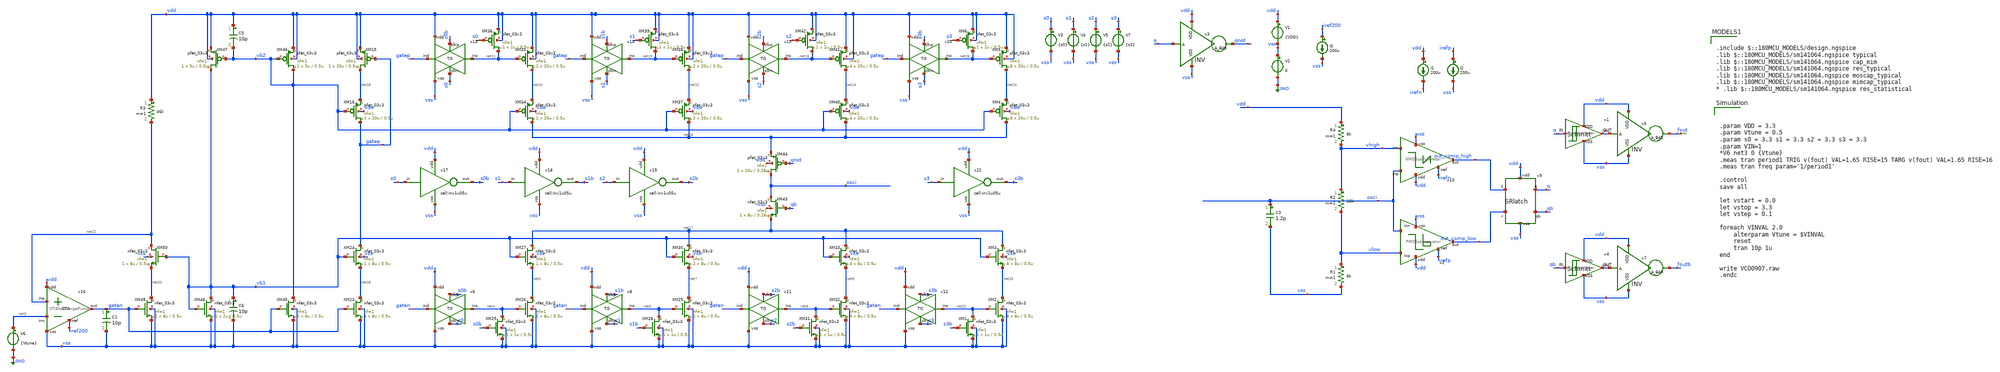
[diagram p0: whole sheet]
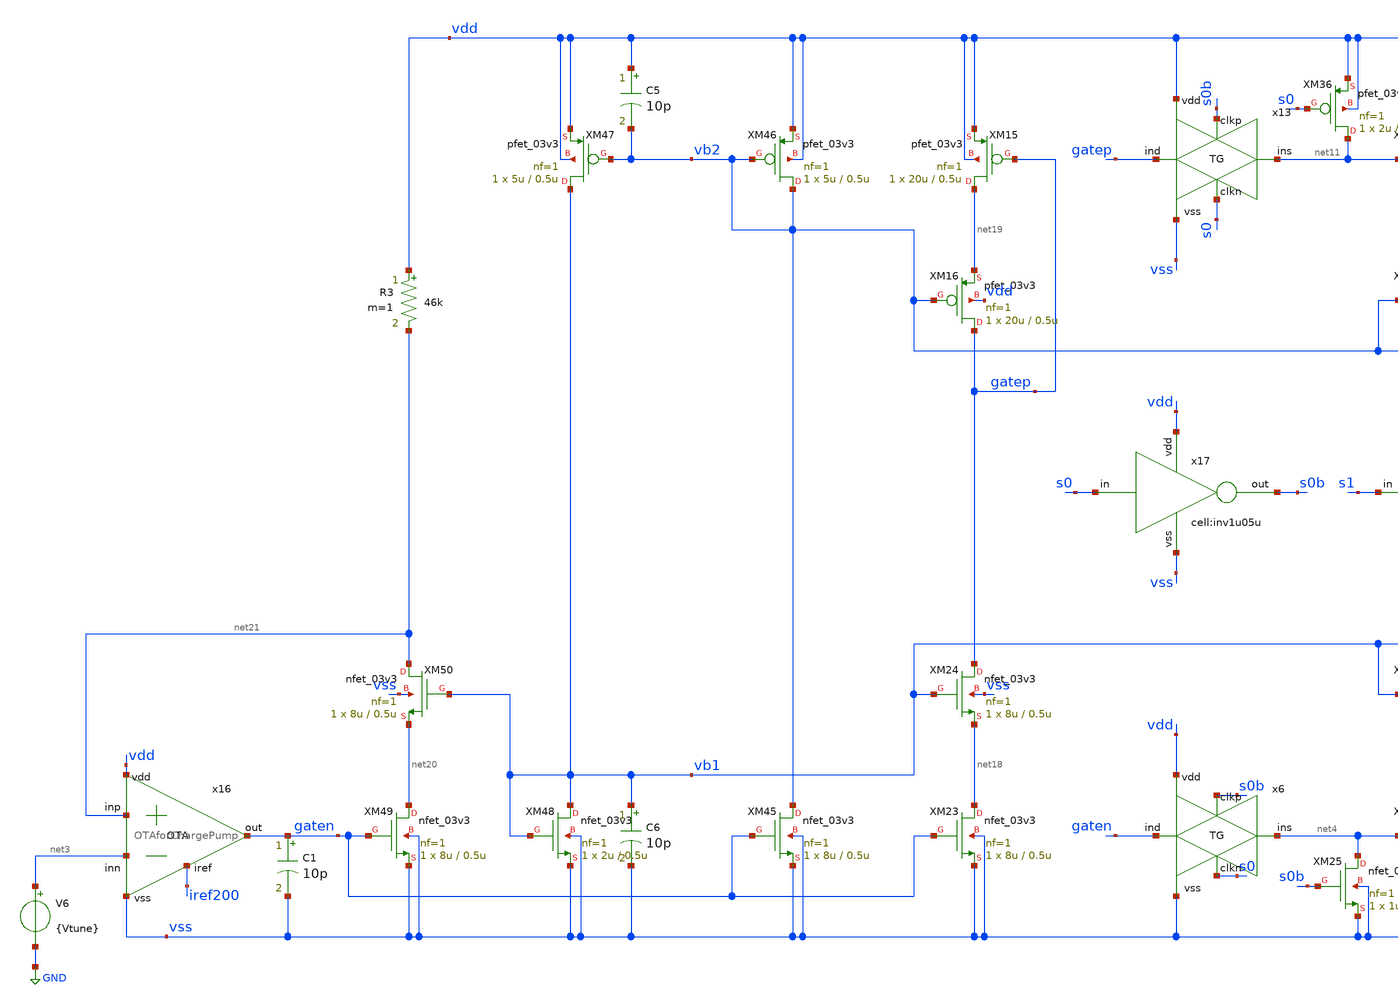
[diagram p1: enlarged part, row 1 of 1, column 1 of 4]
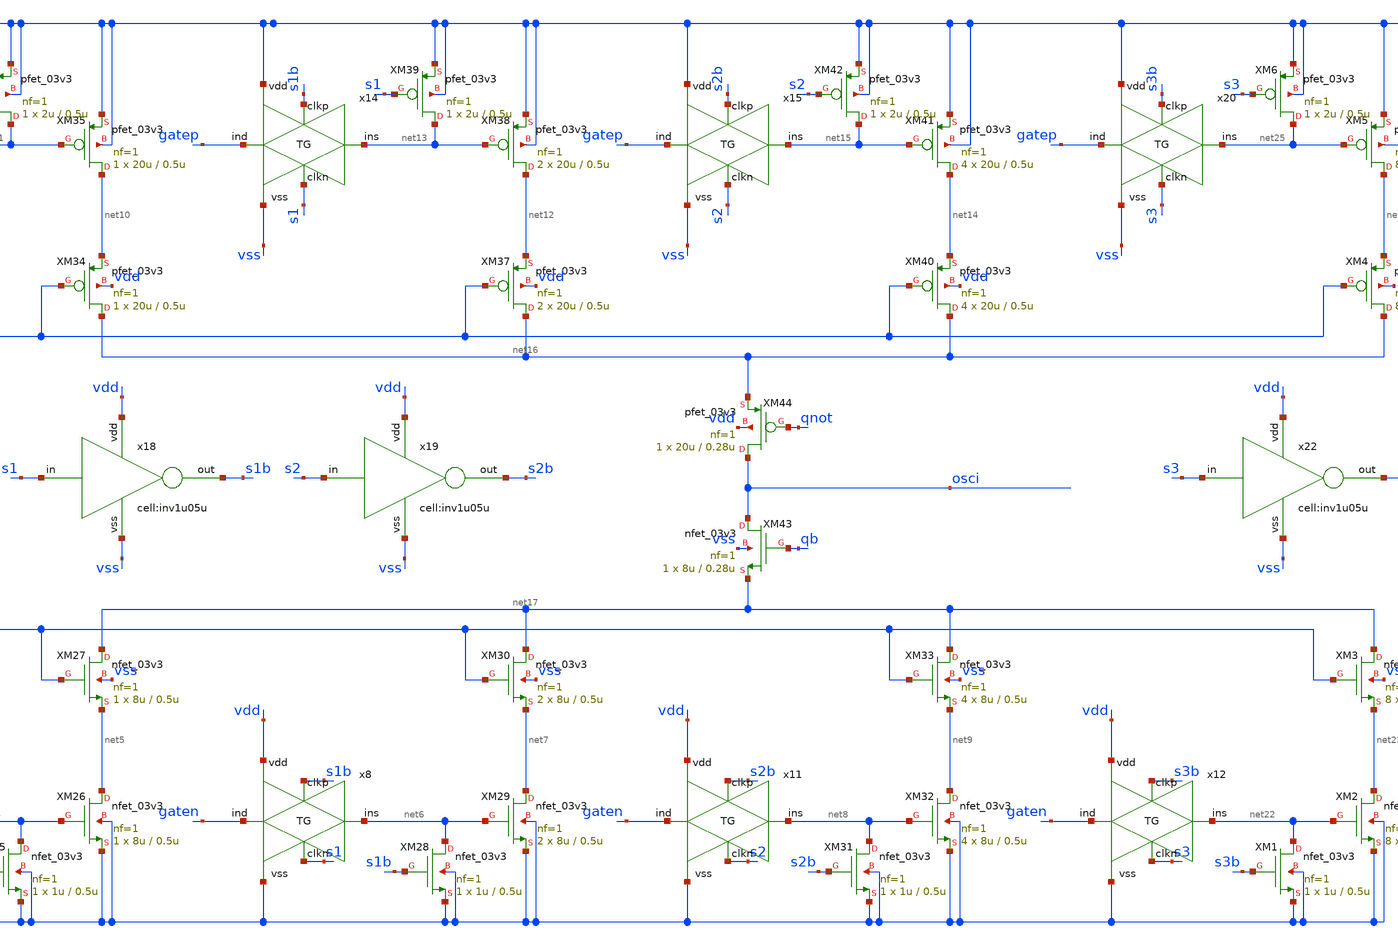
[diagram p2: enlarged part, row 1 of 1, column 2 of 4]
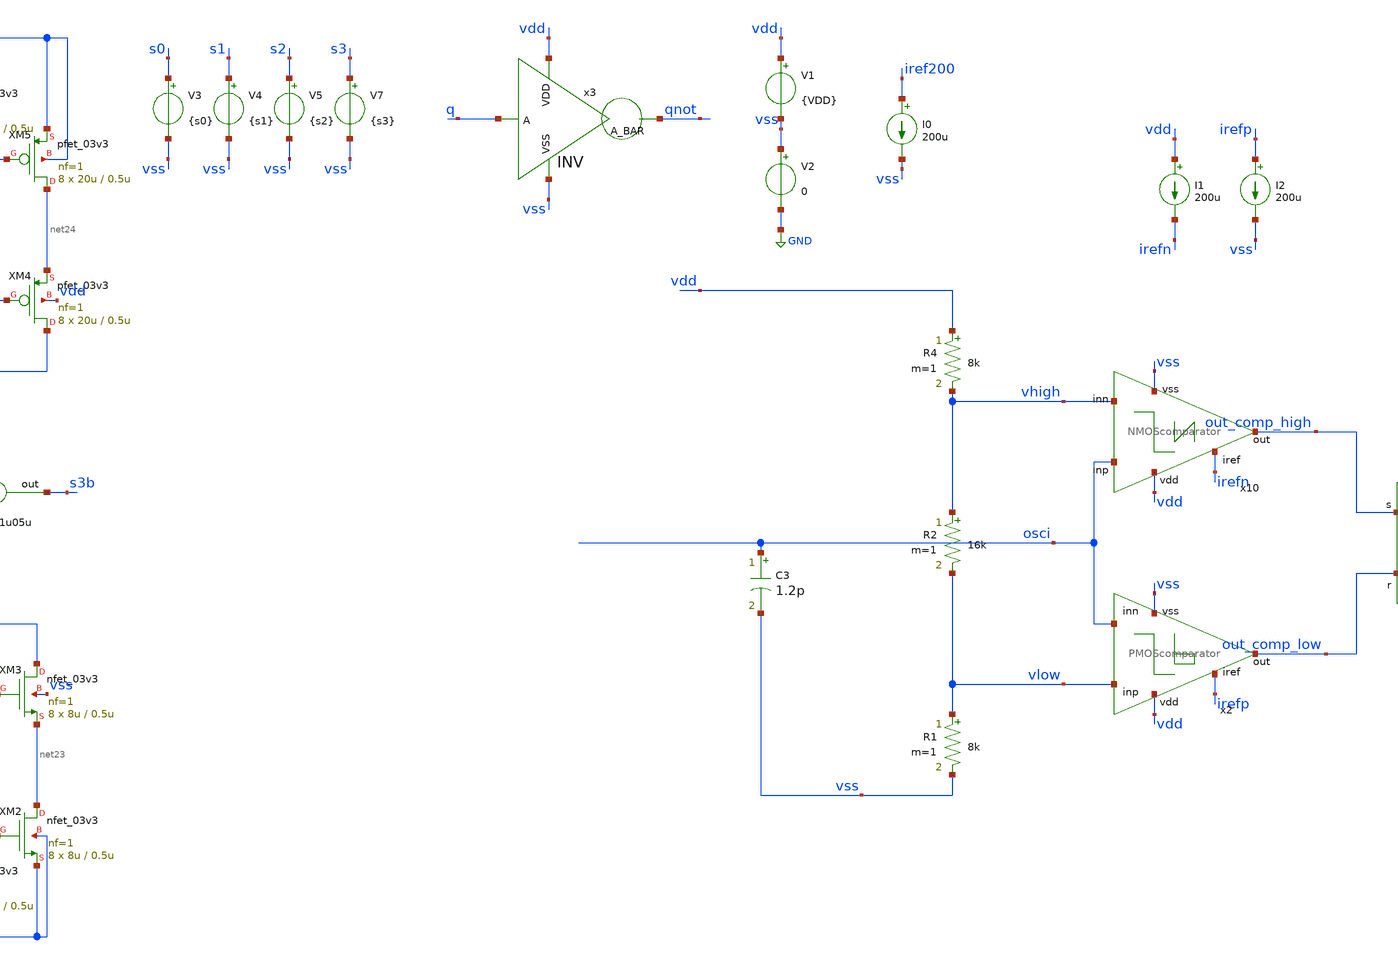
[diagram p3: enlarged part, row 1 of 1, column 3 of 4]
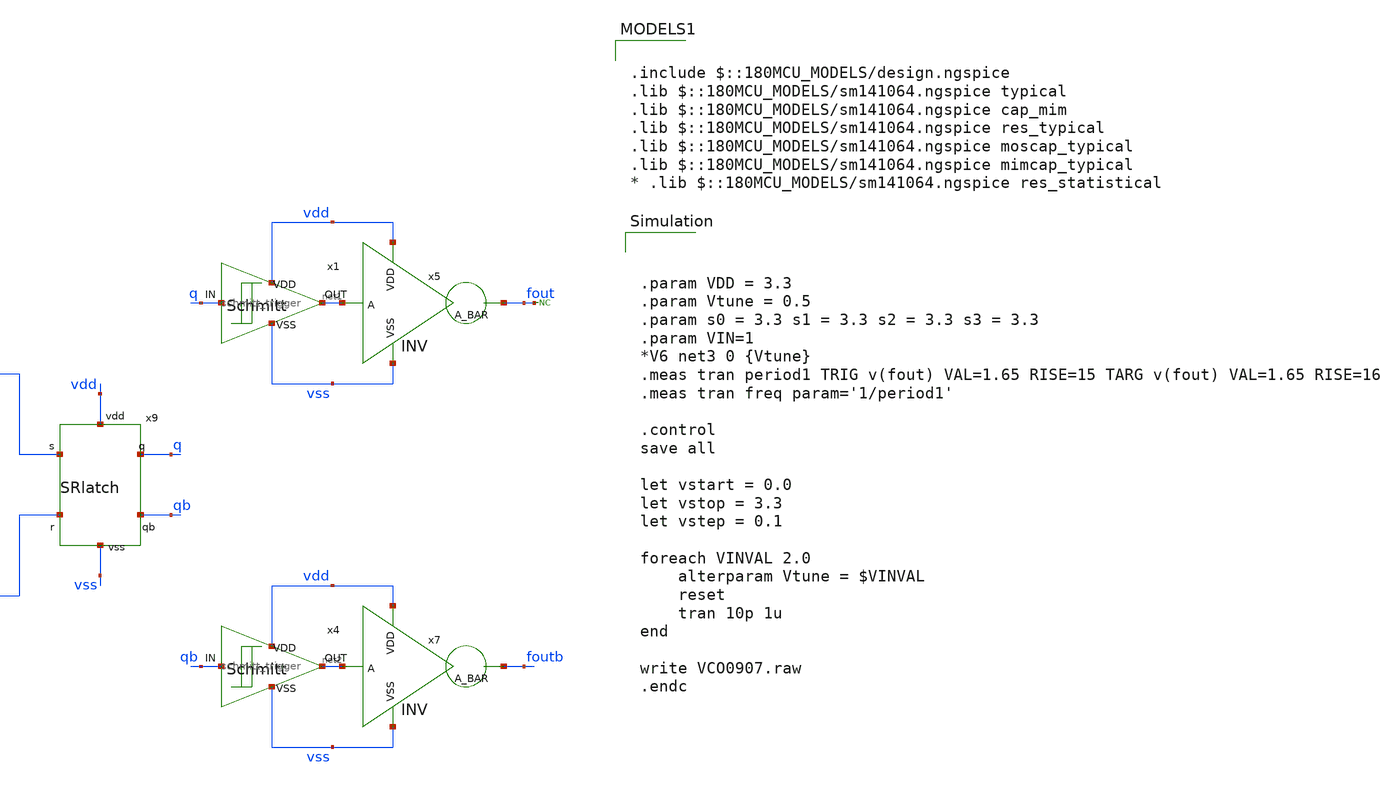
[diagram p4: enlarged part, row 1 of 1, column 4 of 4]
** sch_path: designs/libs/qw_tb_analog/VCOfinal_tb/VCOfinal_tb.sch
**.subckt VCOfinal_tb
V1 vdd vss {VDD}
V2 vss GND 0
I1 vdd irefn 200u
I2 irefp vss 200u
R1 vlow vss 8k m=1
R2 vhigh vlow 16k m=1
R4 vdd vhigh 8k m=1
x9 vdd out_comp_high q qb out_comp_low vss SRlatch
x2 vdd irefp vlow out_comp_low osci vss PMOScomparator
x10 vdd osci out_comp_high vhigh irefn vss NMOScomparator
x3 vdd q qnot vss INV
x1 q net1 vdd vss schmitt_trigger
x4 qb net2 vdd vss schmitt_trigger
x5 vdd net1 fout vss INV
x7 vdd net2 foutb vss INV
V6 net3 GND {Vtune}
I0 iref200 vss 200u
* noconn fout
V3 s0 vss {s0}
V4 s1 vss {s1}
V5 s2 vss {s2}
C3 osci vss 1.2p m=1
V7 s3 vss {s3}
XM25 net4 s0b vss vss nfet_03v3 L=0.5u W=1u nf=1 ad='int((nf+1)/2) * W/nf * 0.18u' as='int((nf+2)/2) * W/nf * 0.18u'
+ pd='2*int((nf+1)/2) * (W/nf + 0.18u)' ps='2*int((nf+2)/2) * (W/nf + 0.18u)' nrd='0.18u / W' nrs='0.18u / W'
+ sa=0 sb=0 sd=0 m=1
XM26 net5 net4 vss vss nfet_03v3 L=0.5u W=8u nf=1 ad='int((nf+1)/2) * W/nf * 0.18u' as='int((nf+2)/2) * W/nf * 0.18u'
+ pd='2*int((nf+1)/2) * (W/nf + 0.18u)' ps='2*int((nf+2)/2) * (W/nf + 0.18u)' nrd='0.18u / W' nrs='0.18u / W'
+ sa=0 sb=0 sd=0 m=1
XM27 net17 vb1 net5 vss nfet_03v3 L=0.5u W=8u nf=1 ad='int((nf+1)/2) * W/nf * 0.18u' as='int((nf+2)/2) * W/nf * 0.18u'
+ pd='2*int((nf+1)/2) * (W/nf + 0.18u)' ps='2*int((nf+2)/2) * (W/nf + 0.18u)' nrd='0.18u / W' nrs='0.18u / W'
+ sa=0 sb=0 sd=0 m=1
XM28 net6 s1b vss vss nfet_03v3 L=0.5u W=1u nf=1 ad='int((nf+1)/2) * W/nf * 0.18u' as='int((nf+2)/2) * W/nf * 0.18u'
+ pd='2*int((nf+1)/2) * (W/nf + 0.18u)' ps='2*int((nf+2)/2) * (W/nf + 0.18u)' nrd='0.18u / W' nrs='0.18u / W'
+ sa=0 sb=0 sd=0 m=1
XM29 net7 net6 vss vss nfet_03v3 L=0.5u W=8u nf=1 ad='int((nf+1)/2) * W/nf * 0.18u' as='int((nf+2)/2) * W/nf * 0.18u'
+ pd='2*int((nf+1)/2) * (W/nf + 0.18u)' ps='2*int((nf+2)/2) * (W/nf + 0.18u)' nrd='0.18u / W' nrs='0.18u / W'
+ sa=0 sb=0 sd=0 m=2
XM30 net17 vb1 net7 vss nfet_03v3 L=0.5u W=8u nf=1 ad='int((nf+1)/2) * W/nf * 0.18u' as='int((nf+2)/2) * W/nf * 0.18u'
+ pd='2*int((nf+1)/2) * (W/nf + 0.18u)' ps='2*int((nf+2)/2) * (W/nf + 0.18u)' nrd='0.18u / W' nrs='0.18u / W'
+ sa=0 sb=0 sd=0 m=2
XM31 net8 s2b vss vss nfet_03v3 L=0.5u W=1u nf=1 ad='int((nf+1)/2) * W/nf * 0.18u' as='int((nf+2)/2) * W/nf * 0.18u'
+ pd='2*int((nf+1)/2) * (W/nf + 0.18u)' ps='2*int((nf+2)/2) * (W/nf + 0.18u)' nrd='0.18u / W' nrs='0.18u / W'
+ sa=0 sb=0 sd=0 m=1
XM32 net9 net8 vss vss nfet_03v3 L=0.5u W=8u nf=1 ad='int((nf+1)/2) * W/nf * 0.18u' as='int((nf+2)/2) * W/nf * 0.18u'
+ pd='2*int((nf+1)/2) * (W/nf + 0.18u)' ps='2*int((nf+2)/2) * (W/nf + 0.18u)' nrd='0.18u / W' nrs='0.18u / W'
+ sa=0 sb=0 sd=0 m=4
XM33 net17 vb1 net9 vss nfet_03v3 L=0.5u W=8u nf=1 ad='int((nf+1)/2) * W/nf * 0.18u' as='int((nf+2)/2) * W/nf * 0.18u'
+ pd='2*int((nf+1)/2) * (W/nf + 0.18u)' ps='2*int((nf+2)/2) * (W/nf + 0.18u)' nrd='0.18u / W' nrs='0.18u / W'
+ sa=0 sb=0 sd=0 m=4
XM34 net16 vb2 net10 vdd pfet_03v3 L=0.5u W=20u nf=1 ad='int((nf+1)/2) * W/nf * 0.18u' as='int((nf+2)/2) * W/nf * 0.18u'
+ pd='2*int((nf+1)/2) * (W/nf + 0.18u)' ps='2*int((nf+2)/2) * (W/nf + 0.18u)' nrd='0.18u / W' nrs='0.18u / W'
+ sa=0 sb=0 sd=0 m=1
XM35 net10 net11 vdd vdd pfet_03v3 L=0.5u W=20u nf=1 ad='int((nf+1)/2) * W/nf * 0.18u' as='int((nf+2)/2) * W/nf * 0.18u'
+ pd='2*int((nf+1)/2) * (W/nf + 0.18u)' ps='2*int((nf+2)/2) * (W/nf + 0.18u)' nrd='0.18u / W' nrs='0.18u / W'
+ sa=0 sb=0 sd=0 m=1
XM36 net11 s0 vdd vdd pfet_03v3 L=0.5u W=2u nf=1 ad='int((nf+1)/2) * W/nf * 0.18u' as='int((nf+2)/2) * W/nf * 0.18u'
+ pd='2*int((nf+1)/2) * (W/nf + 0.18u)' ps='2*int((nf+2)/2) * (W/nf + 0.18u)' nrd='0.18u / W' nrs='0.18u / W'
+ sa=0 sb=0 sd=0 m=1
XM37 net16 vb2 net12 vdd pfet_03v3 L=0.5u W=20u nf=1 ad='int((nf+1)/2) * W/nf * 0.18u' as='int((nf+2)/2) * W/nf * 0.18u'
+ pd='2*int((nf+1)/2) * (W/nf + 0.18u)' ps='2*int((nf+2)/2) * (W/nf + 0.18u)' nrd='0.18u / W' nrs='0.18u / W'
+ sa=0 sb=0 sd=0 m=2
XM38 net12 net13 vdd vdd pfet_03v3 L=0.5u W=20u nf=1 ad='int((nf+1)/2) * W/nf * 0.18u' as='int((nf+2)/2) * W/nf * 0.18u'
+ pd='2*int((nf+1)/2) * (W/nf + 0.18u)' ps='2*int((nf+2)/2) * (W/nf + 0.18u)' nrd='0.18u / W' nrs='0.18u / W'
+ sa=0 sb=0 sd=0 m=2
XM39 net13 s1 vdd vdd pfet_03v3 L=0.5u W=2u nf=1 ad='int((nf+1)/2) * W/nf * 0.18u' as='int((nf+2)/2) * W/nf * 0.18u'
+ pd='2*int((nf+1)/2) * (W/nf + 0.18u)' ps='2*int((nf+2)/2) * (W/nf + 0.18u)' nrd='0.18u / W' nrs='0.18u / W'
+ sa=0 sb=0 sd=0 m=1
XM40 net16 vb2 net14 vdd pfet_03v3 L=0.5u W=20u nf=1 ad='int((nf+1)/2) * W/nf * 0.18u' as='int((nf+2)/2) * W/nf * 0.18u'
+ pd='2*int((nf+1)/2) * (W/nf + 0.18u)' ps='2*int((nf+2)/2) * (W/nf + 0.18u)' nrd='0.18u / W' nrs='0.18u / W'
+ sa=0 sb=0 sd=0 m=4
XM41 net14 net15 vdd vdd pfet_03v3 L=0.5u W=20u nf=1 ad='int((nf+1)/2) * W/nf * 0.18u' as='int((nf+2)/2) * W/nf * 0.18u'
+ pd='2*int((nf+1)/2) * (W/nf + 0.18u)' ps='2*int((nf+2)/2) * (W/nf + 0.18u)' nrd='0.18u / W' nrs='0.18u / W'
+ sa=0 sb=0 sd=0 m=4
XM42 net15 s2 vdd vdd pfet_03v3 L=0.5u W=2u nf=1 ad='int((nf+1)/2) * W/nf * 0.18u' as='int((nf+2)/2) * W/nf * 0.18u'
+ pd='2*int((nf+1)/2) * (W/nf + 0.18u)' ps='2*int((nf+2)/2) * (W/nf + 0.18u)' nrd='0.18u / W' nrs='0.18u / W'
+ sa=0 sb=0 sd=0 m=1
XM43 osci qb net17 vss nfet_03v3 L=0.28u W=8u nf=1 ad='int((nf+1)/2) * W/nf * 0.18u' as='int((nf+2)/2) * W/nf * 0.18u'
+ pd='2*int((nf+1)/2) * (W/nf + 0.18u)' ps='2*int((nf+2)/2) * (W/nf + 0.18u)' nrd='0.18u / W' nrs='0.18u / W'
+ sa=0 sb=0 sd=0 m=1
XM44 osci qnot net16 vdd pfet_03v3 L=0.28u W=20u nf=1 ad='int((nf+1)/2) * W/nf * 0.18u' as='int((nf+2)/2) * W/nf * 0.18u'
+ pd='2*int((nf+1)/2) * (W/nf + 0.18u)' ps='2*int((nf+2)/2) * (W/nf + 0.18u)' nrd='0.18u / W' nrs='0.18u / W'
+ sa=0 sb=0 sd=0 m=1
XM15 net19 gatep vdd vdd pfet_03v3 L=0.5u W=20u nf=1 ad='int((nf+1)/2) * W/nf * 0.18u' as='int((nf+2)/2) * W/nf * 0.18u'
+ pd='2*int((nf+1)/2) * (W/nf + 0.18u)' ps='2*int((nf+2)/2) * (W/nf + 0.18u)' nrd='0.18u / W' nrs='0.18u / W'
+ sa=0 sb=0 sd=0 m=1
XM16 gatep vb2 net19 vdd pfet_03v3 L=0.5u W=20u nf=1 ad='int((nf+1)/2) * W/nf * 0.18u' as='int((nf+2)/2) * W/nf * 0.18u'
+ pd='2*int((nf+1)/2) * (W/nf + 0.18u)' ps='2*int((nf+2)/2) * (W/nf + 0.18u)' nrd='0.18u / W' nrs='0.18u / W'
+ sa=0 sb=0 sd=0 m=1
XM23 net18 gaten vss vss nfet_03v3 L=0.5u W=8u nf=1 ad='int((nf+1)/2) * W/nf * 0.18u' as='int((nf+2)/2) * W/nf * 0.18u'
+ pd='2*int((nf+1)/2) * (W/nf + 0.18u)' ps='2*int((nf+2)/2) * (W/nf + 0.18u)' nrd='0.18u / W' nrs='0.18u / W'
+ sa=0 sb=0 sd=0 m=1
XM24 gatep vb1 net18 vss nfet_03v3 L=0.5u W=8u nf=1 ad='int((nf+1)/2) * W/nf * 0.18u' as='int((nf+2)/2) * W/nf * 0.18u'
+ pd='2*int((nf+1)/2) * (W/nf + 0.18u)' ps='2*int((nf+2)/2) * (W/nf + 0.18u)' nrd='0.18u / W' nrs='0.18u / W'
+ sa=0 sb=0 sd=0 m=1
XM45 vb2 gaten vss vss nfet_03v3 L=0.5u W=8u nf=1 ad='int((nf+1)/2) * W/nf * 0.18u' as='int((nf+2)/2) * W/nf * 0.18u'
+ pd='2*int((nf+1)/2) * (W/nf + 0.18u)' ps='2*int((nf+2)/2) * (W/nf + 0.18u)' nrd='0.18u / W' nrs='0.18u / W'
+ sa=0 sb=0 sd=0 m=1
XM46 vb2 vb2 vdd vdd pfet_03v3 L=0.5u W=5u nf=1 ad='int((nf+1)/2) * W/nf * 0.18u' as='int((nf+2)/2) * W/nf * 0.18u'
+ pd='2*int((nf+1)/2) * (W/nf + 0.18u)' ps='2*int((nf+2)/2) * (W/nf + 0.18u)' nrd='0.18u / W' nrs='0.18u / W'
+ sa=0 sb=0 sd=0 m=1
XM47 vb1 vb2 vdd vdd pfet_03v3 L=0.5u W=5u nf=1 ad='int((nf+1)/2) * W/nf * 0.18u' as='int((nf+2)/2) * W/nf * 0.18u'
+ pd='2*int((nf+1)/2) * (W/nf + 0.18u)' ps='2*int((nf+2)/2) * (W/nf + 0.18u)' nrd='0.18u / W' nrs='0.18u / W'
+ sa=0 sb=0 sd=0 m=1
XM48 vb1 vb1 vss vss nfet_03v3 L=0.5u W=2u nf=1 ad='int((nf+1)/2) * W/nf * 0.18u' as='int((nf+2)/2) * W/nf * 0.18u'
+ pd='2*int((nf+1)/2) * (W/nf + 0.18u)' ps='2*int((nf+2)/2) * (W/nf + 0.18u)' nrd='0.18u / W' nrs='0.18u / W'
+ sa=0 sb=0 sd=0 m=1
XM49 net20 gaten vss vss nfet_03v3 L=0.5u W=8u nf=1 ad='int((nf+1)/2) * W/nf * 0.18u' as='int((nf+2)/2) * W/nf * 0.18u'
+ pd='2*int((nf+1)/2) * (W/nf + 0.18u)' ps='2*int((nf+2)/2) * (W/nf + 0.18u)' nrd='0.18u / W' nrs='0.18u / W'
+ sa=0 sb=0 sd=0 m=1
XM50 net21 vb1 net20 vss nfet_03v3 L=0.5u W=8u nf=1 ad='int((nf+1)/2) * W/nf * 0.18u' as='int((nf+2)/2) * W/nf * 0.18u'
+ pd='2*int((nf+1)/2) * (W/nf + 0.18u)' ps='2*int((nf+2)/2) * (W/nf + 0.18u)' nrd='0.18u / W' nrs='0.18u / W'
+ sa=0 sb=0 sd=0 m=1
x16 vdd iref200 net21 net3 gaten vss OTAforChargePump
R3 vdd net21 46k m=1
C1 gaten vss 10p m=1
C5 vdd vb2 10p m=1
x17 s0 vdd s0b vss inv1u05u
C6 vb1 vss 10p m=1
x18 s1 vdd s1b vss inv1u05u
x19 s2 vdd s2b vss inv1u05u
XM1 net22 s3b vss vss nfet_03v3 L=0.5u W=1u nf=1 ad='int((nf+1)/2) * W/nf * 0.18u' as='int((nf+2)/2) * W/nf * 0.18u'
+ pd='2*int((nf+1)/2) * (W/nf + 0.18u)' ps='2*int((nf+2)/2) * (W/nf + 0.18u)' nrd='0.18u / W' nrs='0.18u / W'
+ sa=0 sb=0 sd=0 m=1
XM2 net23 net22 vss vss nfet_03v3 L=0.5u W=8u nf=1 ad='int((nf+1)/2) * W/nf * 0.18u' as='int((nf+2)/2) * W/nf * 0.18u'
+ pd='2*int((nf+1)/2) * (W/nf + 0.18u)' ps='2*int((nf+2)/2) * (W/nf + 0.18u)' nrd='0.18u / W' nrs='0.18u / W'
+ sa=0 sb=0 sd=0 m=8
XM3 net17 vb1 net23 vss nfet_03v3 L=0.5u W=8u nf=1 ad='int((nf+1)/2) * W/nf * 0.18u' as='int((nf+2)/2) * W/nf * 0.18u'
+ pd='2*int((nf+1)/2) * (W/nf + 0.18u)' ps='2*int((nf+2)/2) * (W/nf + 0.18u)' nrd='0.18u / W' nrs='0.18u / W'
+ sa=0 sb=0 sd=0 m=8
XM4 net16 vb2 net24 vdd pfet_03v3 L=0.5u W=20u nf=1 ad='int((nf+1)/2) * W/nf * 0.18u' as='int((nf+2)/2) * W/nf * 0.18u'
+ pd='2*int((nf+1)/2) * (W/nf + 0.18u)' ps='2*int((nf+2)/2) * (W/nf + 0.18u)' nrd='0.18u / W' nrs='0.18u / W'
+ sa=0 sb=0 sd=0 m=8
XM5 net24 net25 vdd vdd pfet_03v3 L=0.5u W=20u nf=1 ad='int((nf+1)/2) * W/nf * 0.18u' as='int((nf+2)/2) * W/nf * 0.18u'
+ pd='2*int((nf+1)/2) * (W/nf + 0.18u)' ps='2*int((nf+2)/2) * (W/nf + 0.18u)' nrd='0.18u / W' nrs='0.18u / W'
+ sa=0 sb=0 sd=0 m=8
XM6 net25 s3 vdd vdd pfet_03v3 L=0.5u W=2u nf=1 ad='int((nf+1)/2) * W/nf * 0.18u' as='int((nf+2)/2) * W/nf * 0.18u'
+ pd='2*int((nf+1)/2) * (W/nf + 0.18u)' ps='2*int((nf+2)/2) * (W/nf + 0.18u)' nrd='0.18u / W' nrs='0.18u / W'
+ sa=0 sb=0 sd=0 m=1
x22 s3 vdd s3b vss inv1u05u
x6 vdd s0b gaten net4 vss s0 TG
x8 vdd s1b gaten net6 vss s1 TG
x11 vdd s2b gaten net8 vss s2 TG
x12 vdd s3b gaten net22 vss s3 TG
x13 vdd s0b gatep net11 vss s0 TG
x14 vdd s1b gatep net13 vss s1 TG
x15 vdd s2b gatep net15 vss s2 TG
x20 vdd s3b gatep net25 vss s3 TG
**** begin user architecture code



.param VDD = 3.3
.param Vtune = 0.5
.param s0 = 3.3 s1 = 3.3 s2 = 3.3 s3 = 3.3
.param VIN=1
*V6 net3 0 {Vtune}
.meas tran period1 TRIG v(fout) VAL=1.65 RISE=15 TARG v(fout) VAL=1.65 RISE=16
.meas tran freq param='1/period1'

.control
save all

let vstart = 0.0
let vstop = 3.3
let vstep = 0.1

foreach VINVAL 2.0
    alterparam Vtune = $VINVAL
    reset
    tran 10p 1u
end

write VCO0907.raw
.endc



.include $::180MCU_MODELS/design.ngspice
.lib $::180MCU_MODELS/sm141064.ngspice typical
.lib $::180MCU_MODELS/sm141064.ngspice cap_mim
.lib $::180MCU_MODELS/sm141064.ngspice res_typical
.lib $::180MCU_MODELS/sm141064.ngspice moscap_typical
.lib $::180MCU_MODELS/sm141064.ngspice mimcap_typical
* .lib $::180MCU_MODELS/sm141064.ngspice res_statistical

**** end user architecture code
**.ends
.GLOBAL GND
.end
